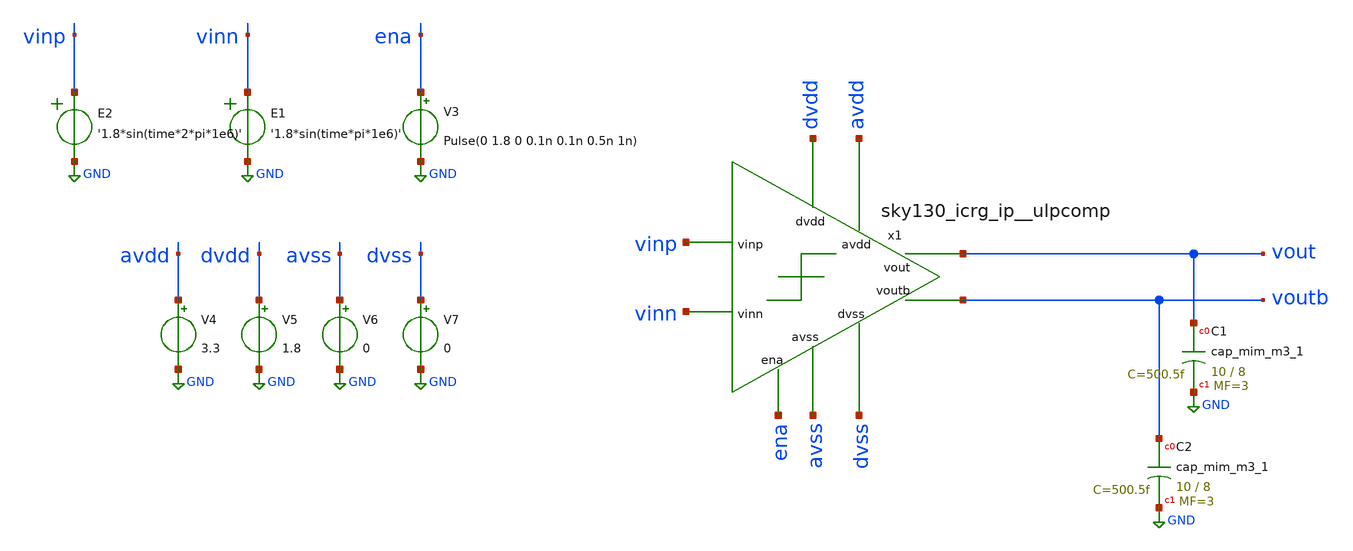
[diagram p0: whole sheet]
** sch_path: cace/tb_propdelay.sch
**.subckt tb_propdelay
V3 ena GND Pulse(0 1.8 0 0.1n 0.1n 0.5n 1n)
V4 avdd GND 3.3
V5 dvdd GND 1.8
V6 avss GND 0
V7 dvss GND 0
E1 vinn GND VOL=' '1.8*sin(time*pi*1e6)' '
E2 vinp GND VOL=' '1.8*sin(time*2*pi*1e6)' '
XC2 voutb GND sky130_fd_pr__cap_mim_m3_1 W=10 L=8 MF=3 m=3
XC1 vout GND sky130_fd_pr__cap_mim_m3_1 W=10 L=8 MF=3 m=3
x1 dvdd avdd ena vinp vinn vout voutb avss dvss sky130_icrg_ip__ulpcomp
**** begin user architecture code


.lib /home/ttuser/pdk/sky130A/libs.tech/combined/sky130.lib.spice {corner}
.option TEMP={temperature}


.control
tran 10n 1u
meas tran trise WHEN V(vout) = [{dvdd} / 2] CROSS=1
let tpd = $&trise

echo $&tpd > {simpath}/{filename}_{N}.data
quit
.endc

**** end user architecture code
**.ends
.GLOBAL GND
.end
